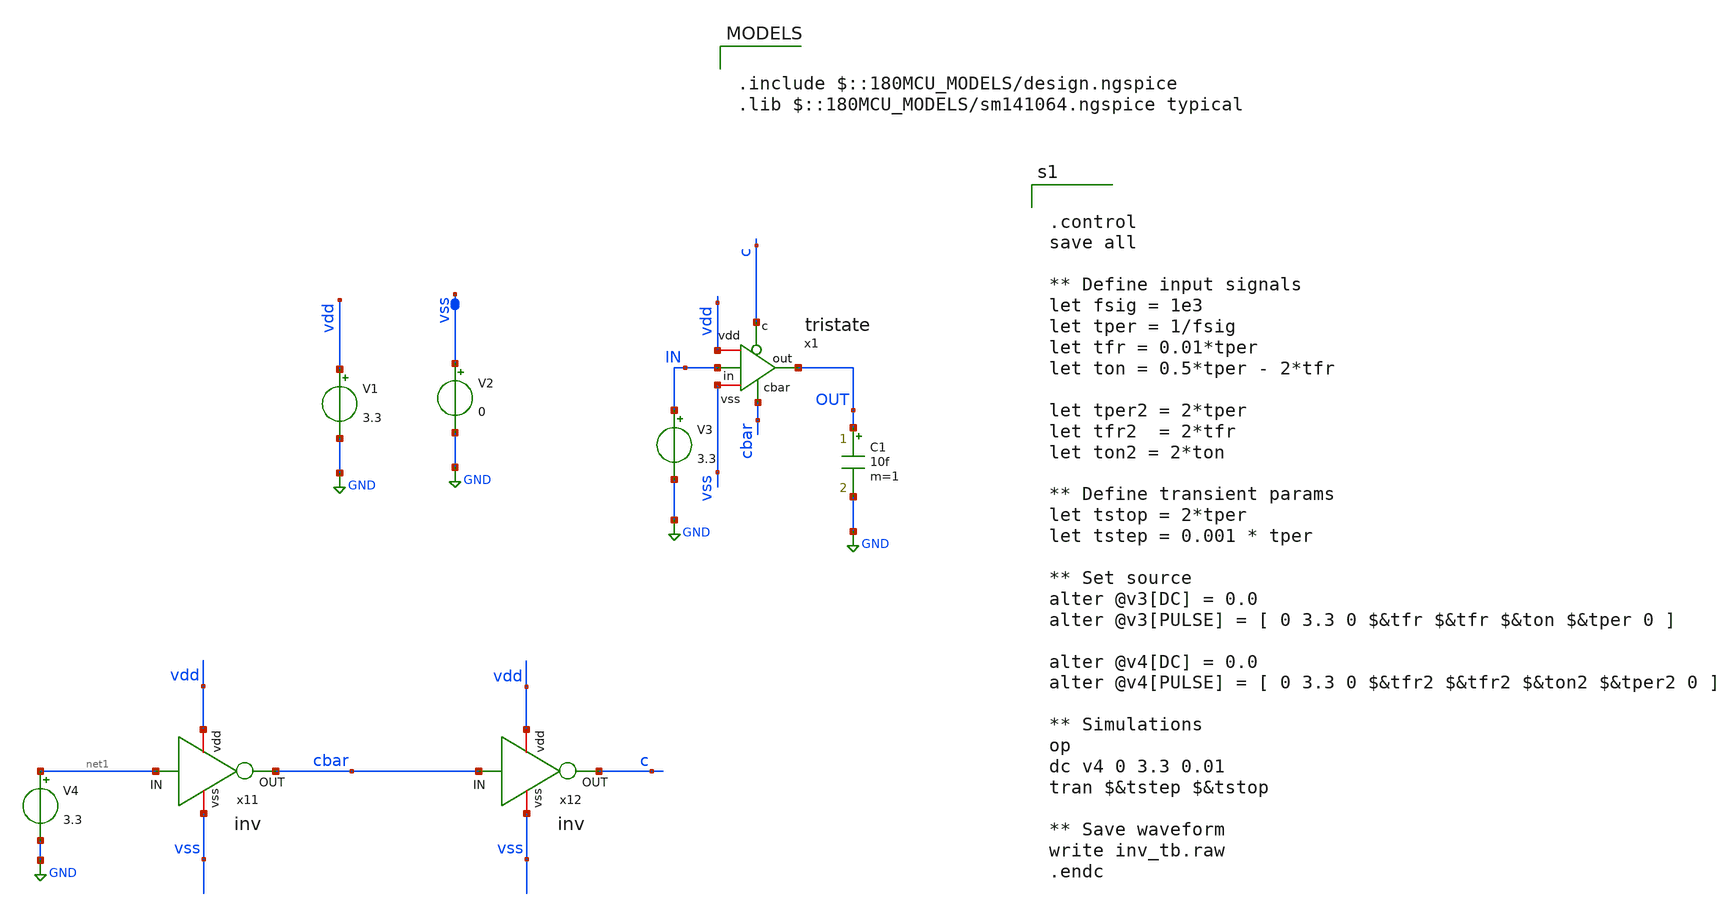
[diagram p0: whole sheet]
** sch_path: tristate_tb.sch
**.subckt tristate_tb
V1 vdd GND 3.3
V2 vss GND 0
V3 IN GND 3.3
C1 OUT GND 10f m=1
x11 vdd net1 cbar vss inv
x12 vdd cbar c vss inv
V4 net1 GND 3.3
x1 vdd c OUT IN cbar vss tristate
**** begin user architecture code

.include $::180MCU_MODELS/design.ngspice
.lib $::180MCU_MODELS/sm141064.ngspice typical



.control
save all

** Define input signals
let fsig = 1e3
let tper = 1/fsig
let tfr = 0.01*tper
let ton = 0.5*tper - 2*tfr

let tper2 = 2*tper
let tfr2  = 2*tfr
let ton2 = 2*ton

** Define transient params
let tstop = 2*tper
let tstep = 0.001 * tper

** Set source
alter @v3[DC] = 0.0
alter @v3[PULSE] = [ 0 3.3 0 $&tfr $&tfr $&ton $&tper 0 ]

alter @v4[DC] = 0.0
alter @v4[PULSE] = [ 0 3.3 0 $&tfr2 $&tfr2 $&ton2 $&tper2 0 ]

** Simulations
op
dc v4 0 3.3 0.01
tran $&tstep $&tstop

** Save waveform
write inv_tb.raw
.endc


**** end user architecture code
**.ends

* expanding   symbol:  inv.sym # of pins=4
** sym_path: inv.sym
** sch_path: inv.sch
.subckt inv vdd IN OUT vss
*.ipin IN
*.opin OUT
*.iopin vdd
*.iopin vss
XM1 OUT IN vss vss nfet_03v3 L=0.28u W=1u nf=1 ad='int((nf+1)/2) * W/nf * 0.18u' as='int((nf+2)/2) * W/nf * 0.18u'
+ pd='2*int((nf+1)/2) * (W/nf + 0.18u)' ps='2*int((nf+2)/2) * (W/nf + 0.18u)' nrd='0.18u / W' nrs='0.18u / W'
+ sa=0 sb=0 sd=0 m=1
XM2 OUT IN vdd vdd pfet_03v3 L=0.28u W=1u nf=1 ad='int((nf+1)/2) * W/nf * 0.18u' as='int((nf+2)/2) * W/nf * 0.18u'
+ pd='2*int((nf+1)/2) * (W/nf + 0.18u)' ps='2*int((nf+2)/2) * (W/nf + 0.18u)' nrd='0.18u / W' nrs='0.18u / W'
+ sa=0 sb=0 sd=0 m=1
.ends


* expanding   symbol:  tristate.sym # of pins=6
** sym_path: tristate.sym
** sch_path: tristate.sch
.subckt tristate vdd c out in cbar vss
*.ipin in
*.opin out
*.iopin vdd
*.iopin vss
*.ipin c
*.ipin cbar
XM1 net1 c vdd vdd pfet_03v3 L=0.28u W=0.42u nf=1 ad='int((nf+1)/2) * W/nf * 0.18u' as='int((nf+2)/2) * W/nf * 0.18u'
+ pd='2*int((nf+1)/2) * (W/nf + 0.18u)' ps='2*int((nf+2)/2) * (W/nf + 0.18u)' nrd='0.18u / W' nrs='0.18u / W'
+ sa=0 sb=0 sd=0 m=1
XM2 out in net1 vdd pfet_03v3 L=0.28u W=0.42u nf=1 ad='int((nf+1)/2) * W/nf * 0.18u' as='int((nf+2)/2) * W/nf * 0.18u'
+ pd='2*int((nf+1)/2) * (W/nf + 0.18u)' ps='2*int((nf+2)/2) * (W/nf + 0.18u)' nrd='0.18u / W' nrs='0.18u / W'
+ sa=0 sb=0 sd=0 m=1
XM3 out in net2 vss nfet_03v3 L=0.28u W=0.42u nf=1 ad='int((nf+1)/2) * W/nf * 0.18u' as='int((nf+2)/2) * W/nf * 0.18u'
+ pd='2*int((nf+1)/2) * (W/nf + 0.18u)' ps='2*int((nf+2)/2) * (W/nf + 0.18u)' nrd='0.18u / W' nrs='0.18u / W'
+ sa=0 sb=0 sd=0 m=1
XM4 net2 cbar vss vss nfet_03v3 L=0.28u W=0.42u nf=1 ad='int((nf+1)/2) * W/nf * 0.18u' as='int((nf+2)/2) * W/nf * 0.18u'
+ pd='2*int((nf+1)/2) * (W/nf + 0.18u)' ps='2*int((nf+2)/2) * (W/nf + 0.18u)' nrd='0.18u / W' nrs='0.18u / W'
+ sa=0 sb=0 sd=0 m=1
.ends

.GLOBAL GND
.end
